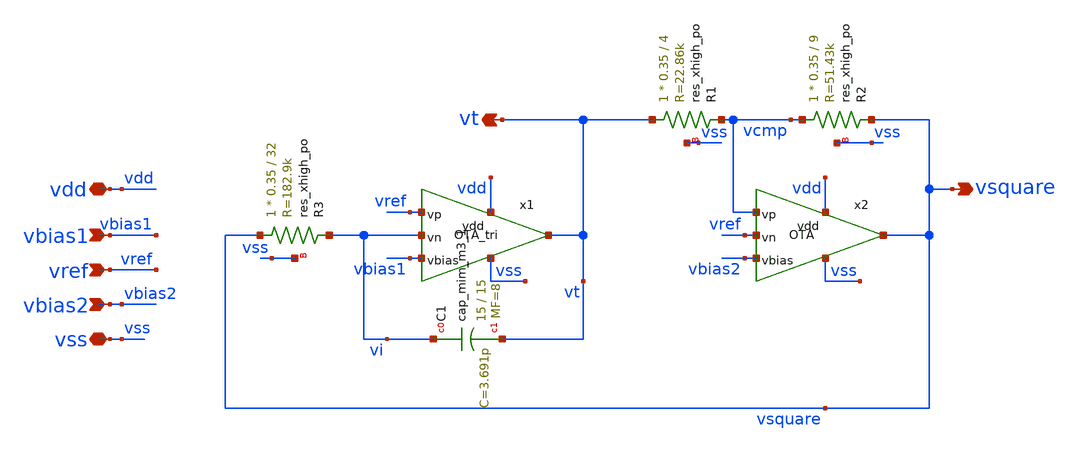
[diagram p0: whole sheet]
** sch_path: xschem/src/triangle/triangle.sch
**.subckt triangle vdd vbias1 vt vref vsquare vss vbias2
*.iopin vdd
*.ipin vbias1
*.opin vt
*.ipin vref
*.opin vsquare
*.iopin vss
*.ipin vbias2
XR3 vsquare vi vss sky130_fd_pr__res_xhigh_po L=32 mult=1 m=1
XR1 vt vcmp vss sky130_fd_pr__res_xhigh_po L=4 mult=1 m=1
XR2 vcmp vsquare vss sky130_fd_pr__res_xhigh_po L=9 mult=1 m=1
x1 vdd vref vi vbias1 vss vt OTA_tri
x2 vdd vcmp vref vbias2 vss vsquare OTA
XC1 vi vt sky130_fd_pr__cap_mim_m3_1 W=15 L=15 MF=8 m=8
**.ends

* expanding   symbol:  src/OTA_tri/OTA_tri.sym # of pins=6
** sym_path: xschem/src/OTA_tri/OTA_tri.sym
** sch_path: xschem/src/OTA_tri/OTA_tri.sch
.subckt OTA_tri vdd vp vn vbias vss vout
*.ipin vp
*.ipin vn
*.ipin vbias
*.iopin vss
*.iopin vdd
*.opin vout
XM1 v1 vp vc vc sky130_fd_pr__pfet_01v8_lvt L=1 W=4 nf=1 ad='int((nf+1)/2) * W/nf * 0.29' as='int((nf+2)/2) * W/nf * 0.29'
+ pd='2*int((nf+1)/2) * (W/nf + 0.29)' ps='2*int((nf+2)/2) * (W/nf + 0.29)' nrd='0.29 / W' nrs='0.29 / W'
+ sa=0 sb=0 sd=0 mult=16 m=16
XM2 vf vn vc vc sky130_fd_pr__pfet_01v8_lvt L=1 W=4 nf=1 ad='int((nf+1)/2) * W/nf * 0.29' as='int((nf+2)/2) * W/nf * 0.29'
+ pd='2*int((nf+1)/2) * (W/nf + 0.29)' ps='2*int((nf+2)/2) * (W/nf + 0.29)' nrd='0.29 / W' nrs='0.29 / W'
+ sa=0 sb=0 sd=0 mult=16 m=16
XM3 vc vbias vdd vdd sky130_fd_pr__pfet_01v8_lvt L=1 W=2 nf=2 ad='int((nf+1)/2) * W/nf * 0.29' as='int((nf+2)/2) * W/nf * 0.29'
+ pd='2*int((nf+1)/2) * (W/nf + 0.29)' ps='2*int((nf+2)/2) * (W/nf + 0.29)' nrd='0.29 / W' nrs='0.29 / W'
+ sa=0 sb=0 sd=0 mult=24 m=24
XM4 v1 vf vss vss sky130_fd_pr__nfet_01v8_lvt L=1 W=1 nf=1 ad='int((nf+1)/2) * W/nf * 0.29' as='int((nf+2)/2) * W/nf * 0.29'
+ pd='2*int((nf+1)/2) * (W/nf + 0.29)' ps='2*int((nf+2)/2) * (W/nf + 0.29)' nrd='0.29 / W' nrs='0.29 / W'
+ sa=0 sb=0 sd=0 mult=16 m=16
XM5 vf vf vss vss sky130_fd_pr__nfet_01v8_lvt L=1 W=1 nf=1 ad='int((nf+1)/2) * W/nf * 0.29' as='int((nf+2)/2) * W/nf * 0.29'
+ pd='2*int((nf+1)/2) * (W/nf + 0.29)' ps='2*int((nf+2)/2) * (W/nf + 0.29)' nrd='0.29 / W' nrs='0.29 / W'
+ sa=0 sb=0 sd=0 mult=16 m=16
XM6 vbias vbias vdd vdd sky130_fd_pr__pfet_01v8_lvt L=1 W=2 nf=2 ad='int((nf+1)/2) * W/nf * 0.29' as='int((nf+2)/2) * W/nf * 0.29'
+ pd='2*int((nf+1)/2) * (W/nf + 0.29)' ps='2*int((nf+2)/2) * (W/nf + 0.29)' nrd='0.29 / W' nrs='0.29 / W'
+ sa=0 sb=0 sd=0 mult=24 m=24
XM7 vout vbias vdd vdd sky130_fd_pr__pfet_01v8_lvt L=1 W=2 nf=3 ad='int((nf+1)/2) * W/nf * 0.29' as='int((nf+2)/2) * W/nf * 0.29'
+ pd='2*int((nf+1)/2) * (W/nf + 0.29)' ps='2*int((nf+2)/2) * (W/nf + 0.29)' nrd='0.29 / W' nrs='0.29 / W'
+ sa=0 sb=0 sd=0 mult=48 m=48
XM8 vout v1 vss vss sky130_fd_pr__nfet_01v8_lvt L=1 W=1 nf=1 ad='int((nf+1)/2) * W/nf * 0.29' as='int((nf+2)/2) * W/nf * 0.29'
+ pd='2*int((nf+1)/2) * (W/nf + 0.29)' ps='2*int((nf+2)/2) * (W/nf + 0.29)' nrd='0.29 / W' nrs='0.29 / W'
+ sa=0 sb=0 sd=0 mult=64 m=64
XC1 net1 vout sky130_fd_pr__cap_mim_m3_1 W=27 L=18 MF=1 m=1
XR1 v1 net1 vss sky130_fd_pr__res_xhigh_po W=0.35 L=1.4 mult=1 m=1
.ends


* expanding   symbol:  src/OTA/OTA.sym # of pins=6
** sym_path: xschem/src/OTA/OTA.sym
** sch_path: xschem/src/OTA/OTA.sch
.subckt OTA vdd vp vn vbias vss vout
*.ipin vp
*.ipin vn
*.ipin vbias
*.iopin vss
*.iopin vdd
*.opin vout
XM1 v1 vp vc vc sky130_fd_pr__pfet_01v8_lvt L=1 W=4 nf=1 ad='int((nf+1)/2) * W/nf * 0.29' as='int((nf+2)/2) * W/nf * 0.29'
+ pd='2*int((nf+1)/2) * (W/nf + 0.29)' ps='2*int((nf+2)/2) * (W/nf + 0.29)' nrd='0.29 / W' nrs='0.29 / W'
+ sa=0 sb=0 sd=0 mult=16 m=16
XM2 vf vn vc vc sky130_fd_pr__pfet_01v8_lvt L=1 W=4 nf=1 ad='int((nf+1)/2) * W/nf * 0.29' as='int((nf+2)/2) * W/nf * 0.29'
+ pd='2*int((nf+1)/2) * (W/nf + 0.29)' ps='2*int((nf+2)/2) * (W/nf + 0.29)' nrd='0.29 / W' nrs='0.29 / W'
+ sa=0 sb=0 sd=0 mult=16 m=16
XM3 vc vbias vdd vdd sky130_fd_pr__pfet_01v8_lvt L=1 W=2 nf=2 ad='int((nf+1)/2) * W/nf * 0.29' as='int((nf+2)/2) * W/nf * 0.29'
+ pd='2*int((nf+1)/2) * (W/nf + 0.29)' ps='2*int((nf+2)/2) * (W/nf + 0.29)' nrd='0.29 / W' nrs='0.29 / W'
+ sa=0 sb=0 sd=0 mult=24 m=24
XM4 v1 vf vss vss sky130_fd_pr__nfet_01v8_lvt L=1 W=1 nf=1 ad='int((nf+1)/2) * W/nf * 0.29' as='int((nf+2)/2) * W/nf * 0.29'
+ pd='2*int((nf+1)/2) * (W/nf + 0.29)' ps='2*int((nf+2)/2) * (W/nf + 0.29)' nrd='0.29 / W' nrs='0.29 / W'
+ sa=0 sb=0 sd=0 mult=16 m=16
XM5 vf vf vss vss sky130_fd_pr__nfet_01v8_lvt L=1 W=1 nf=1 ad='int((nf+1)/2) * W/nf * 0.29' as='int((nf+2)/2) * W/nf * 0.29'
+ pd='2*int((nf+1)/2) * (W/nf + 0.29)' ps='2*int((nf+2)/2) * (W/nf + 0.29)' nrd='0.29 / W' nrs='0.29 / W'
+ sa=0 sb=0 sd=0 mult=16 m=16
XM6 vbias vbias vdd vdd sky130_fd_pr__pfet_01v8_lvt L=1 W=2 nf=2 ad='int((nf+1)/2) * W/nf * 0.29' as='int((nf+2)/2) * W/nf * 0.29'
+ pd='2*int((nf+1)/2) * (W/nf + 0.29)' ps='2*int((nf+2)/2) * (W/nf + 0.29)' nrd='0.29 / W' nrs='0.29 / W'
+ sa=0 sb=0 sd=0 mult=24 m=24
XM7 vout vbias vdd vdd sky130_fd_pr__pfet_01v8_lvt L=1 W=2 nf=2 ad='int((nf+1)/2) * W/nf * 0.29' as='int((nf+2)/2) * W/nf * 0.29'
+ pd='2*int((nf+1)/2) * (W/nf + 0.29)' ps='2*int((nf+2)/2) * (W/nf + 0.29)' nrd='0.29 / W' nrs='0.29 / W'
+ sa=0 sb=0 sd=0 mult=48 m=48
XM8 vout v1 vss vss sky130_fd_pr__nfet_01v8_lvt L=1 W=1 nf=1 ad='int((nf+1)/2) * W/nf * 0.29' as='int((nf+2)/2) * W/nf * 0.29'
+ pd='2*int((nf+1)/2) * (W/nf + 0.29)' ps='2*int((nf+2)/2) * (W/nf + 0.29)' nrd='0.29 / W' nrs='0.29 / W'
+ sa=0 sb=0 sd=0 mult=64 m=64
XR1 v1 net1 vss sky130_fd_pr__res_xhigh_po W=0.35 L=0.5 mult=1 m=1
XC2 net1 vout sky130_fd_pr__cap_mim_m3_1 W=14 L=14 MF=1 m=1
.ends

.end
